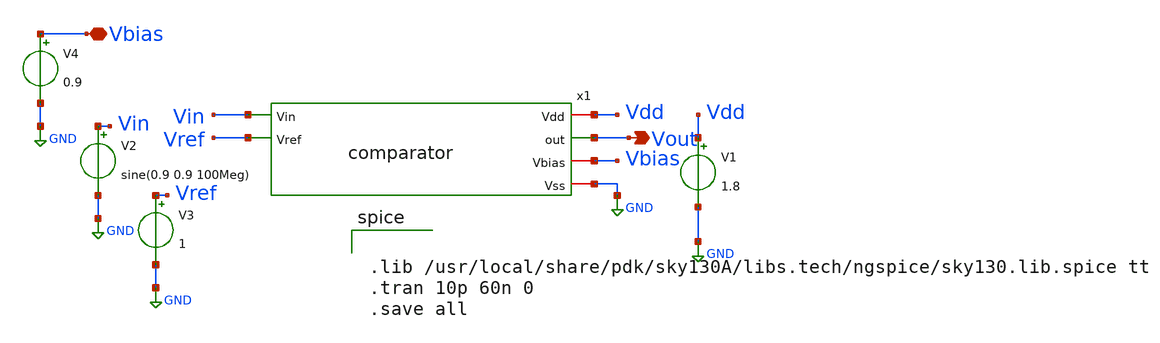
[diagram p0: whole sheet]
** sch_path: Week5/images/pre-layout_1bitADC/tb_comparator.sch
**.subckt tb_comparator Vbias Vout
*.iopin Vbias
*.opin Vout
V1 Vdd GND 1.8
V2 Vin GND sine(0.9 0.9 100Meg)
V3 Vref GND 1
x1 Vdd Vout Vin Vref Vbias GND comparator
V4 Vbias GND 0.9
**** begin user architecture code


.lib /usr/local/share/pdk/sky130A/libs.tech/ngspice/sky130.lib.spice tt
.tran 10p 60n 0
.save all


**** end user architecture code
**.ends

* expanding   symbol:  comparator.sym # of pins=6
** sym_path: Week5/images/pre-layout_1bitADC/comparator.sym
** sch_path: Week5/images/pre-layout_1bitADC/comparator.sch
.subckt comparator Vdd out Vin Vref Vbias Vss
*.iopin Vdd
*.iopin Vss
*.opin out
*.ipin Vin
*.ipin Vref
*.iopin Vbias
XM1 net1 Vbias Vss Vss sky130_fd_pr__nfet_01v8 L=0.15 W=0.8 nf=1 ad='int((nf+1)/2) * W/nf * 0.29' as='int((nf+2)/2) * W/nf * 0.29'
+ pd='2*int((nf+1)/2) * (W/nf + 0.29)' ps='2*int((nf+2)/2) * (W/nf + 0.29)' nrd='0.29 / W' nrs='0.29 / W'
+ sa=0 sb=0 sd=0 mult=1 m=1
XM2 net2 Vin net1 Vss sky130_fd_pr__nfet_01v8 L=0.15 W=0.8 nf=1 ad='int((nf+1)/2) * W/nf * 0.29' as='int((nf+2)/2) * W/nf * 0.29'
+ pd='2*int((nf+1)/2) * (W/nf + 0.29)' ps='2*int((nf+2)/2) * (W/nf + 0.29)' nrd='0.29 / W' nrs='0.29 / W'
+ sa=0 sb=0 sd=0 mult=1 m=1
XM3 net3 Vref net1 Vss sky130_fd_pr__nfet_01v8 L=0.15 W=0.8 nf=1 ad='int((nf+1)/2) * W/nf * 0.29' as='int((nf+2)/2) * W/nf * 0.29'
+ pd='2*int((nf+1)/2) * (W/nf + 0.29)' ps='2*int((nf+2)/2) * (W/nf + 0.29)' nrd='0.29 / W' nrs='0.29 / W'
+ sa=0 sb=0 sd=0 mult=1 m=1
XM4 net3 net2 Vdd Vdd sky130_fd_pr__pfet_01v8 L=0.15 W=0.8 nf=1 ad='int((nf+1)/2) * W/nf * 0.29' as='int((nf+2)/2) * W/nf * 0.29'
+ pd='2*int((nf+1)/2) * (W/nf + 0.29)' ps='2*int((nf+2)/2) * (W/nf + 0.29)' nrd='0.29 / W' nrs='0.29 / W'
+ sa=0 sb=0 sd=0 mult=1 m=1
XM5 net2 net2 Vdd Vdd sky130_fd_pr__pfet_01v8 L=0.15 W=0.8 nf=1 ad='int((nf+1)/2) * W/nf * 0.29' as='int((nf+2)/2) * W/nf * 0.29'
+ pd='2*int((nf+1)/2) * (W/nf + 0.29)' ps='2*int((nf+2)/2) * (W/nf + 0.29)' nrd='0.29 / W' nrs='0.29 / W'
+ sa=0 sb=0 sd=0 mult=1 m=1
XM6 out net3 Vdd Vdd sky130_fd_pr__pfet_01v8 L=0.15 W=0.8 nf=1 ad='int((nf+1)/2) * W/nf * 0.29' as='int((nf+2)/2) * W/nf * 0.29'
+ pd='2*int((nf+1)/2) * (W/nf + 0.29)' ps='2*int((nf+2)/2) * (W/nf + 0.29)' nrd='0.29 / W' nrs='0.29 / W'
+ sa=0 sb=0 sd=0 mult=1 m=1
XM9 out net3 Vss Vss sky130_fd_pr__nfet_01v8 L=0.15 W=0.8 nf=1 ad='int((nf+1)/2) * W/nf * 0.29' as='int((nf+2)/2) * W/nf * 0.29'
+ pd='2*int((nf+1)/2) * (W/nf + 0.29)' ps='2*int((nf+2)/2) * (W/nf + 0.29)' nrd='0.29 / W' nrs='0.29 / W'
+ sa=0 sb=0 sd=0 mult=1 m=1
.ends

.GLOBAL GND
.end
